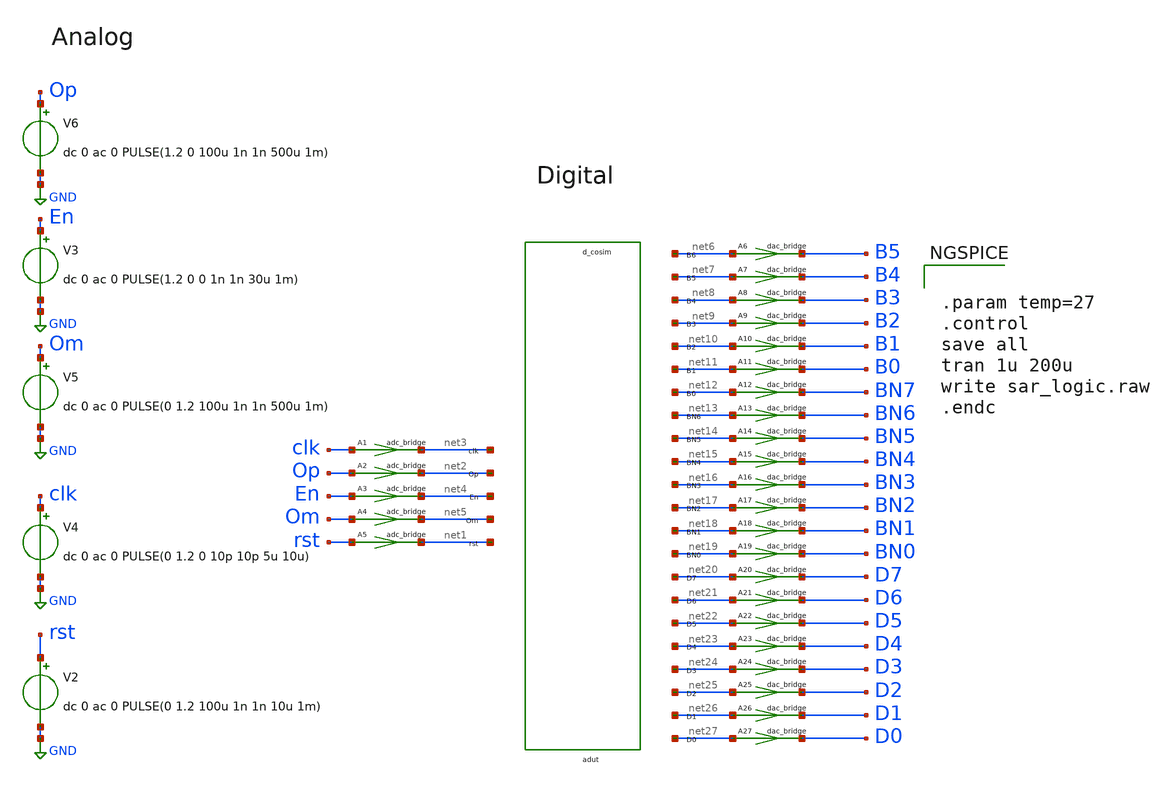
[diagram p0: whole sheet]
** sch_path: part_4_SAR_ADC/sar_logic_tb_docker.sch
* Copyright 2024 IHP PDK Authors
**.subckt sar_logic_tb_docker
V3 En GND dc 0 ac 0 PULSE(1.2 0 0 1n 1n 30u 1m)
V6 Op GND dc 0 ac 0 PULSE(1.2 0 100u 1n 1n 500u 1m)
V2 rst GND dc 0 ac 0 PULSE(0 1.2 100u 1n 1n 10u 1m)
V5 Om GND dc 0 ac 0 PULSE(0 1.2 100u 1n 1n 500u 1m)
V4 clk GND dc 0 ac 0 PULSE(0 1.2 0 10p 10p 5u 10u)
adut [ net3 net2 net4 net5 net1 ] [ net6 net7 net8 net9 net10 net11 net12 net13 net14 net15 net16
+ net17 net18 net19 net20 net21 net22 net23 net24 net25 net26 net27 ] null dut
.model dut d_cosim simulation=./sar_logic.so
A1 [ clk ] [ net3 ] adc1
.model adc1 adc_bridge in_low=0.4 in_high=0.6
A2 [ Op ] [ net2 ] adc1
.model adc1 adc_bridge in_low=0.4 in_high=0.6
A3 [ En ] [ net4 ] adc1
.model adc1 adc_bridge in_low=0.4 in_high=0.6
A4 [ Om ] [ net5 ] adc1
.model adc1 adc_bridge in_low=0.4 in_high=0.6
A5 [ rst ] [ net1 ] adc1
.model adc1 adc_bridge in_low=0.4 in_high=0.6
A6 [ net6 ] [ B5 ] dac1
.model dac1 dac_bridge out_low=0 out_high=1.2
A7 [ net7 ] [ B4 ] dac1
.model dac1 dac_bridge out_low=0 out_high=1.2
A8 [ net8 ] [ B3 ] dac1
.model dac1 dac_bridge out_low=0 out_high=1.2
A9 [ net9 ] [ B2 ] dac1
.model dac1 dac_bridge out_low=0 out_high=1.2
A10 [ net10 ] [ B1 ] dac1
.model dac1 dac_bridge out_low=0 out_high=1.2
A11 [ net11 ] [ B0 ] dac1
.model dac1 dac_bridge out_low=0 out_high=1.2
A12 [ net12 ] [ BN7 ] dac1
.model dac1 dac_bridge out_low=0 out_high=1.2
A13 [ net13 ] [ BN6 ] dac1
.model dac1 dac_bridge out_low=0 out_high=1.2
A14 [ net14 ] [ BN5 ] dac1
.model dac1 dac_bridge out_low=0 out_high=1.2
A15 [ net15 ] [ BN4 ] dac1
.model dac1 dac_bridge out_low=0 out_high=1.2
A16 [ net16 ] [ BN3 ] dac1
.model dac1 dac_bridge out_low=0 out_high=1.2
A17 [ net17 ] [ BN2 ] dac1
.model dac1 dac_bridge out_low=0 out_high=1.2
A18 [ net18 ] [ BN1 ] dac1
.model dac1 dac_bridge out_low=0 out_high=1.2
A19 [ net19 ] [ BN0 ] dac1
.model dac1 dac_bridge out_low=0 out_high=1.2
A20 [ net20 ] [ D7 ] dac1
.model dac1 dac_bridge out_low=0 out_high=1.2
A21 [ net21 ] [ D6 ] dac1
.model dac1 dac_bridge out_low=0 out_high=1.2
A22 [ net22 ] [ D5 ] dac1
.model dac1 dac_bridge out_low=0 out_high=1.2
A23 [ net23 ] [ D4 ] dac1
.model dac1 dac_bridge out_low=0 out_high=1.2
A24 [ net24 ] [ D3 ] dac1
.model dac1 dac_bridge out_low=0 out_high=1.2
A25 [ net25 ] [ D2 ] dac1
.model dac1 dac_bridge out_low=0 out_high=1.2
A26 [ net26 ] [ D1 ] dac1
.model dac1 dac_bridge out_low=0 out_high=1.2
A27 [ net27 ] [ D0 ] dac1
.model dac1 dac_bridge out_low=0 out_high=1.2
**** begin user architecture code


.param temp=27
.control
save all
tran 1u 200u
write sar_logic.raw
.endc


**** end user architecture code
**.ends
.GLOBAL GND
.end
